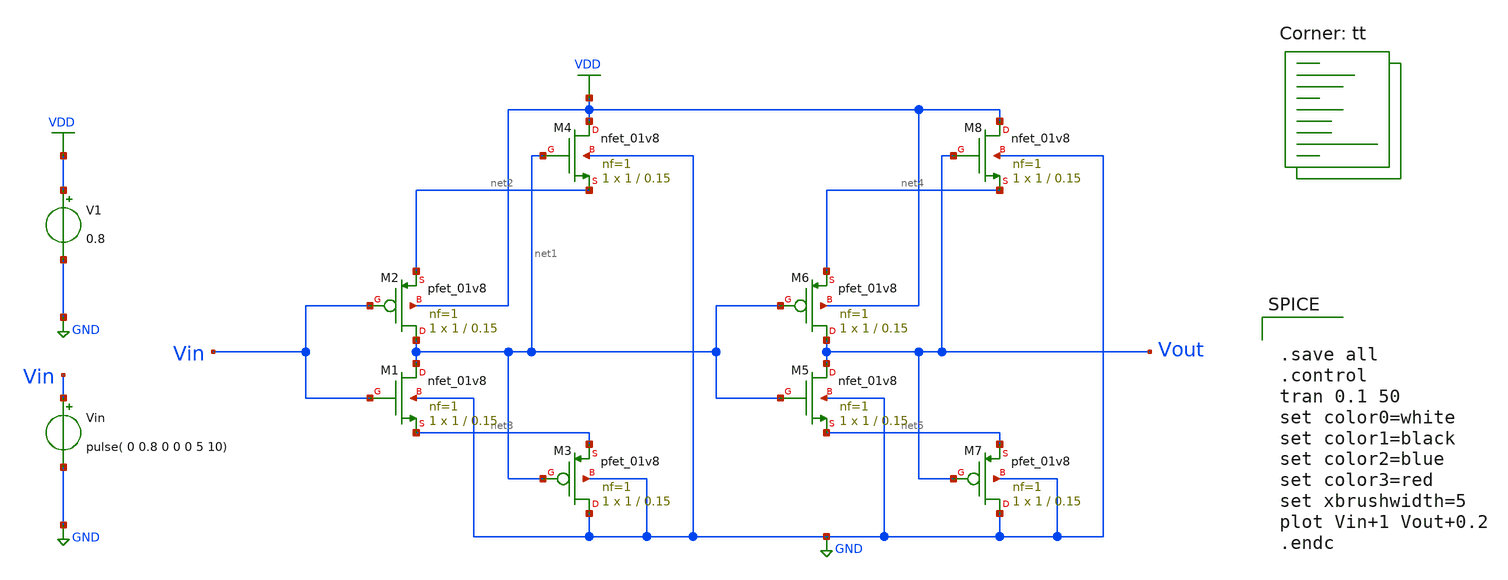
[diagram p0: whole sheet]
** sch_path: dls_buffer.sch
**.subckt dls_buffer
XM1 net1 Vin net3 GND sky130_fd_pr__nfet_01v8 L=0.15 W=1 nf=1 ad='int((nf+1)/2) * W/nf * 0.29' as='int((nf+2)/2) * W/nf * 0.29'
+ pd='2*int((nf+1)/2) * (W/nf + 0.29)' ps='2*int((nf+2)/2) * (W/nf + 0.29)' nrd='0.29 / W' nrs='0.29 / W'
+ sa=0 sb=0 sd=0 mult=1 m=1
XM2 net1 Vin net2 VDD sky130_fd_pr__pfet_01v8 L=0.15 W=1 nf=1 ad='int((nf+1)/2) * W/nf * 0.29' as='int((nf+2)/2) * W/nf * 0.29'
+ pd='2*int((nf+1)/2) * (W/nf + 0.29)' ps='2*int((nf+2)/2) * (W/nf + 0.29)' nrd='0.29 / W' nrs='0.29 / W'
+ sa=0 sb=0 sd=0 mult=1 m=1
V1 VDD GND 0.8
Vin Vin GND pulse( 0 0.8 0 0 0 5 10)
XM3 GND net1 net3 GND sky130_fd_pr__pfet_01v8 L=0.15 W=1 nf=1 ad='int((nf+1)/2) * W/nf * 0.29' as='int((nf+2)/2) * W/nf * 0.29'
+ pd='2*int((nf+1)/2) * (W/nf + 0.29)' ps='2*int((nf+2)/2) * (W/nf + 0.29)' nrd='0.29 / W' nrs='0.29 / W'
+ sa=0 sb=0 sd=0 mult=1 m=1
XM4 VDD net1 net2 GND sky130_fd_pr__nfet_01v8 L=0.15 W=1 nf=1 ad='int((nf+1)/2) * W/nf * 0.29' as='int((nf+2)/2) * W/nf * 0.29'
+ pd='2*int((nf+1)/2) * (W/nf + 0.29)' ps='2*int((nf+2)/2) * (W/nf + 0.29)' nrd='0.29 / W' nrs='0.29 / W'
+ sa=0 sb=0 sd=0 mult=1 m=1
XM5 Vout net1 net5 GND sky130_fd_pr__nfet_01v8 L=0.15 W=1 nf=1 ad='int((nf+1)/2) * W/nf * 0.29' as='int((nf+2)/2) * W/nf * 0.29'
+ pd='2*int((nf+1)/2) * (W/nf + 0.29)' ps='2*int((nf+2)/2) * (W/nf + 0.29)' nrd='0.29 / W' nrs='0.29 / W'
+ sa=0 sb=0 sd=0 mult=1 m=1
XM6 Vout net1 net4 VDD sky130_fd_pr__pfet_01v8 L=0.15 W=1 nf=1 ad='int((nf+1)/2) * W/nf * 0.29' as='int((nf+2)/2) * W/nf * 0.29'
+ pd='2*int((nf+1)/2) * (W/nf + 0.29)' ps='2*int((nf+2)/2) * (W/nf + 0.29)' nrd='0.29 / W' nrs='0.29 / W'
+ sa=0 sb=0 sd=0 mult=1 m=1
XM7 GND Vout net5 GND sky130_fd_pr__pfet_01v8 L=0.15 W=1 nf=1 ad='int((nf+1)/2) * W/nf * 0.29' as='int((nf+2)/2) * W/nf * 0.29'
+ pd='2*int((nf+1)/2) * (W/nf + 0.29)' ps='2*int((nf+2)/2) * (W/nf + 0.29)' nrd='0.29 / W' nrs='0.29 / W'
+ sa=0 sb=0 sd=0 mult=1 m=1
XM8 VDD Vout net4 GND sky130_fd_pr__nfet_01v8 L=0.15 W=1 nf=1 ad='int((nf+1)/2) * W/nf * 0.29' as='int((nf+2)/2) * W/nf * 0.29'
+ pd='2*int((nf+1)/2) * (W/nf + 0.29)' ps='2*int((nf+2)/2) * (W/nf + 0.29)' nrd='0.29 / W' nrs='0.29 / W'
+ sa=0 sb=0 sd=0 mult=1 m=1
**** begin user architecture code
.lib $::SKYWATER_MODELS/sky130.lib.spice tt


.save all
.control
tran 0.1 50
set color0=white
set color1=black
set color2=blue
set color3=red
set xbrushwidth=5
plot Vin+1 Vout+0.2
.endc



**** end user architecture code
**.ends
.GLOBAL VDD
.GLOBAL GND
.end
